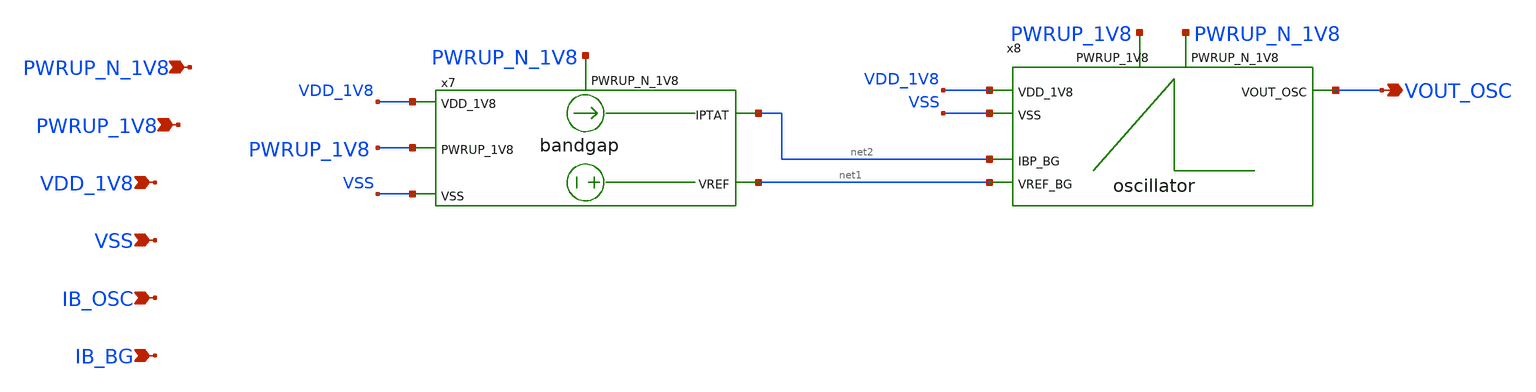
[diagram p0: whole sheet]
** sch_path: design/LELO_GR01_SKY130A/oscillator_tb.sch
**.subckt oscillator_tb VSS VDD_1V8 IB_OSC IB_BG VOUT_OSC PWRUP_N_1V8 PWRUP_1V8
*.ipin VSS
*.ipin VDD_1V8
*.ipin IB_OSC
*.ipin IB_BG
*.opin VOUT_OSC
*.ipin PWRUP_N_1V8
*.ipin PWRUP_1V8
x7 net2 net1 PWRUP_1V8 VDD_1V8 VSS PWRUP_N_1V8 bandgap
x8 VOUT_OSC VDD_1V8 VSS net2 net1 PWRUP_1V8 PWRUP_N_1V8 oscillator
**.ends
.end
